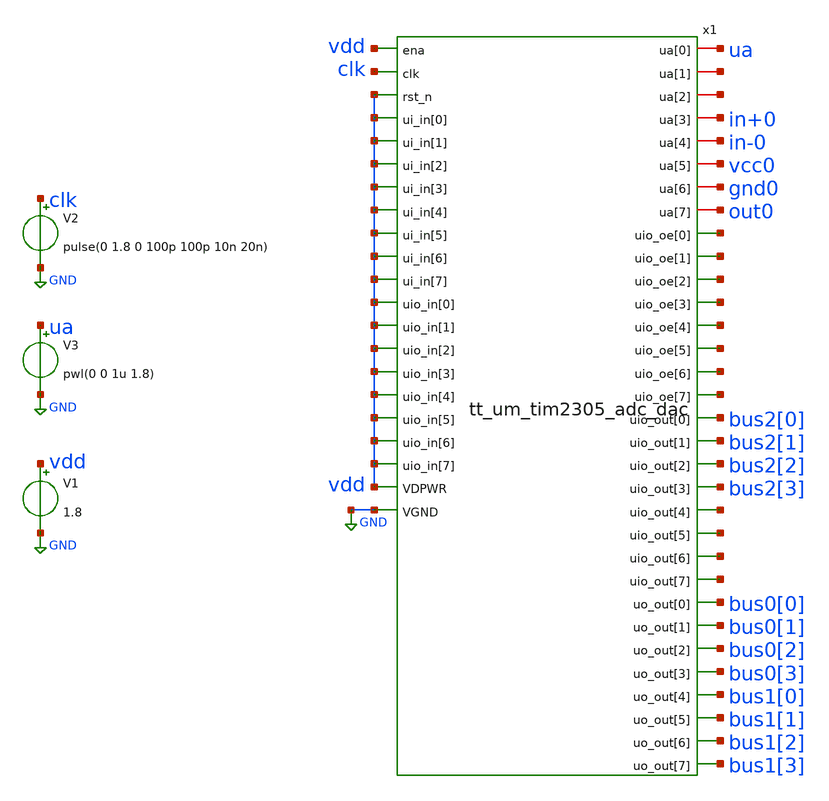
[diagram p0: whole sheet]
** sch_path: xschem/top_tb.sch
**.subckt top_tb
V1 vdd GND 1.8
V3 ua GND pwl(0 0 1u 1.8)
V2 clk GND pulse(0 1.8 0 100p 100p 10n 20n)
x1 ua net1 net2 in+0 in-0 vcc0 gnd0 vdd out0 clk vdd net3 vdd net4 vdd net5 net6 vdd vdd net7 vdd
+ net8 vdd net9 net10 vdd vdd bus2[0] vdd bus2[1] vdd bus2[2] vdd bus2[3] net11 vdd net12 vdd net13 vdd
+ vdd net14 vdd bus0[0] vdd bus0[1] GND bus0[2] bus0[3] bus1[0] bus1[1] bus1[2] bus1[3]
+ tt_um_tim2305_adc_dac
**** begin user architecture code


.tran 100p 1u
.save all
.lib /home/ttuser/pdk/sky130A/libs.tech/ngspice/sky130.lib.spice tt


**** end user architecture code
**.ends

* expanding   symbol:
*+  /home/ttuser/Documents/github_project/adc_dac2/xschem/tt_um_tim2305_adc_dac.sym # of pins=53
** sym_path: xschem/tile_pinout.sym
.include [abs_sym_path tt_um_tim2305_adc_dac.cir]
.GLOBAL GND
.end
